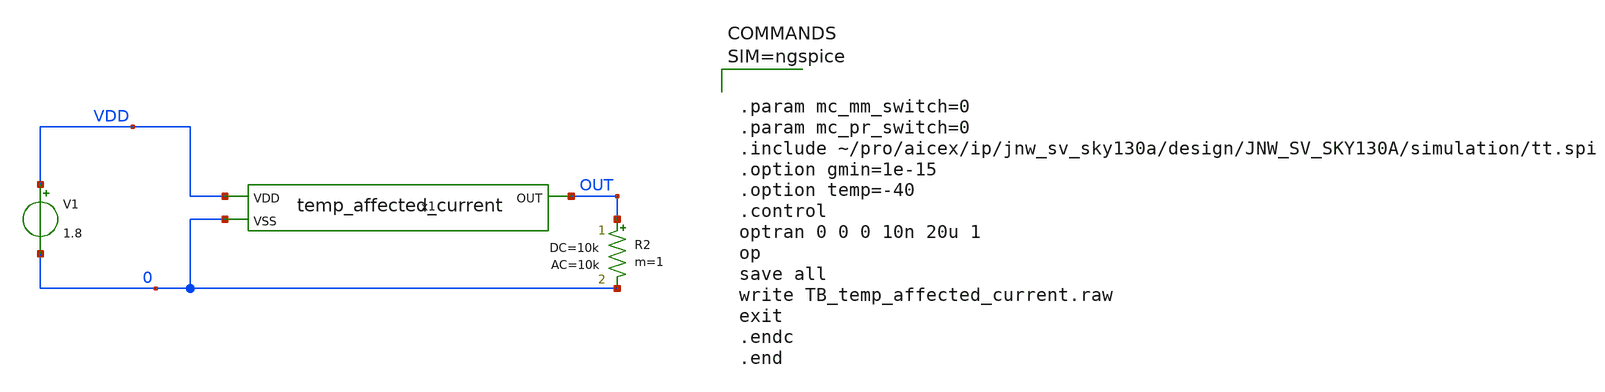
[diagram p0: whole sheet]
** sch_path: design/JNW_GR06_SKY130A/TB_temp_affected_current.sch
**.subckt TB_temp_affected_current
x1 VDD OUT 0 temp_affected_current
V1 VDD 0 1.8
R2 OUT 0 10k ac=10k m=1
**** begin user architecture code



.param mc_mm_switch=0
.param mc_pr_switch=0
.include ~/pro/aicex/ip/jnw_sv_sky130a/design/JNW_SV_SKY130A/simulation/tt.spi
.option gmin=1e-15
.option temp=-40
.control
optran 0 0 0 10n 20u 1
op
save all
write TB_temp_affected_current.raw
exit
.endc
.end



**** end user architecture code
**.ends
.end
